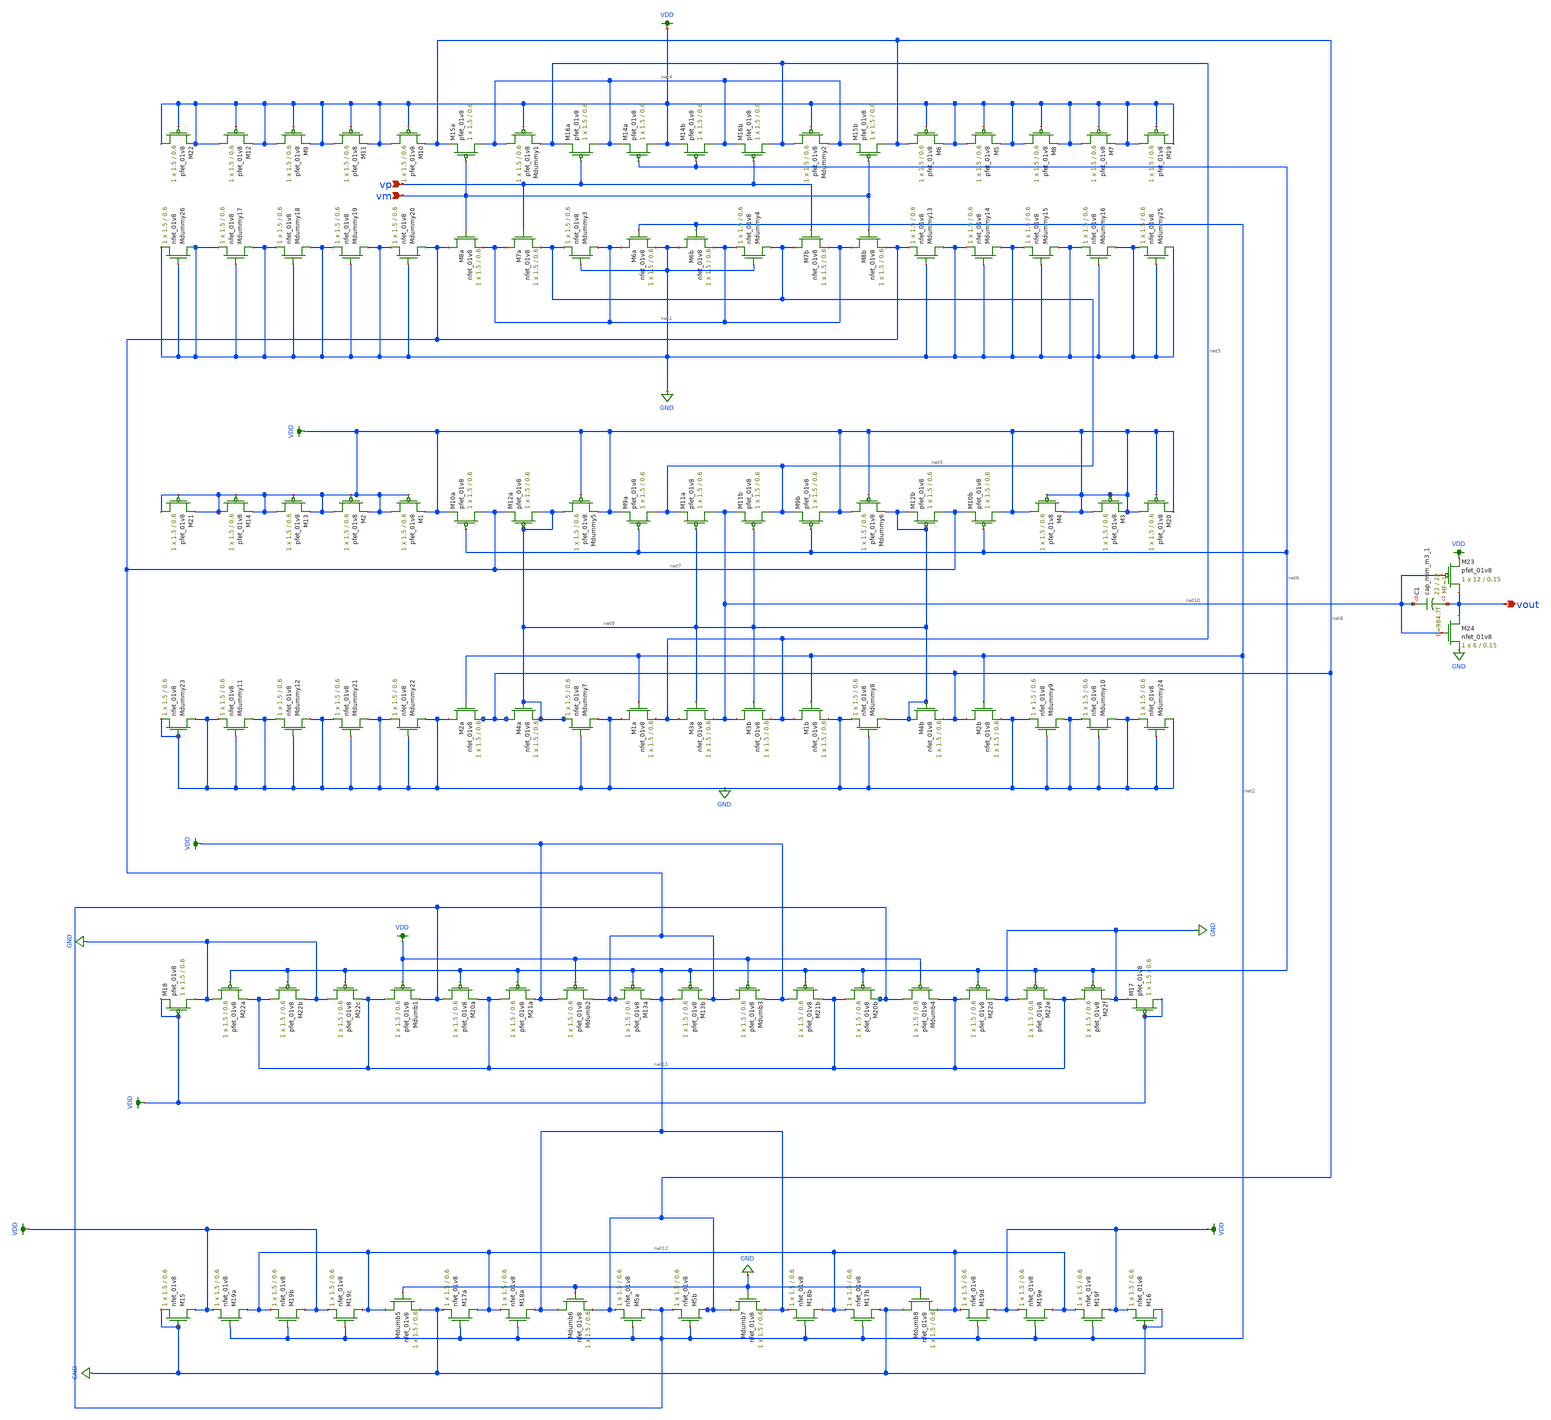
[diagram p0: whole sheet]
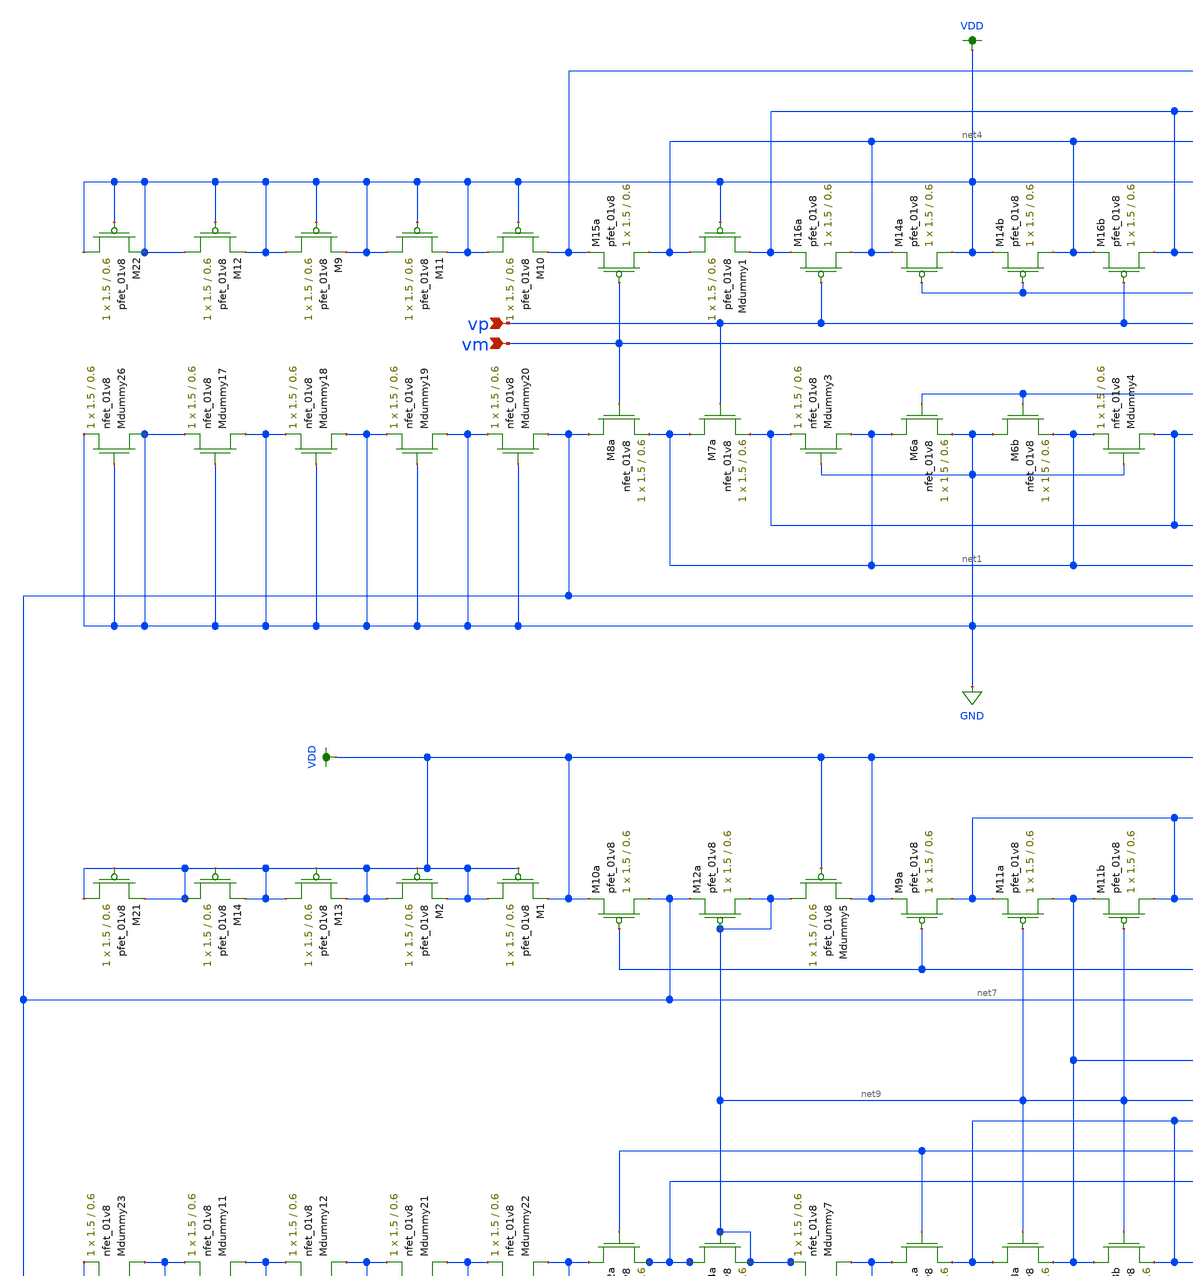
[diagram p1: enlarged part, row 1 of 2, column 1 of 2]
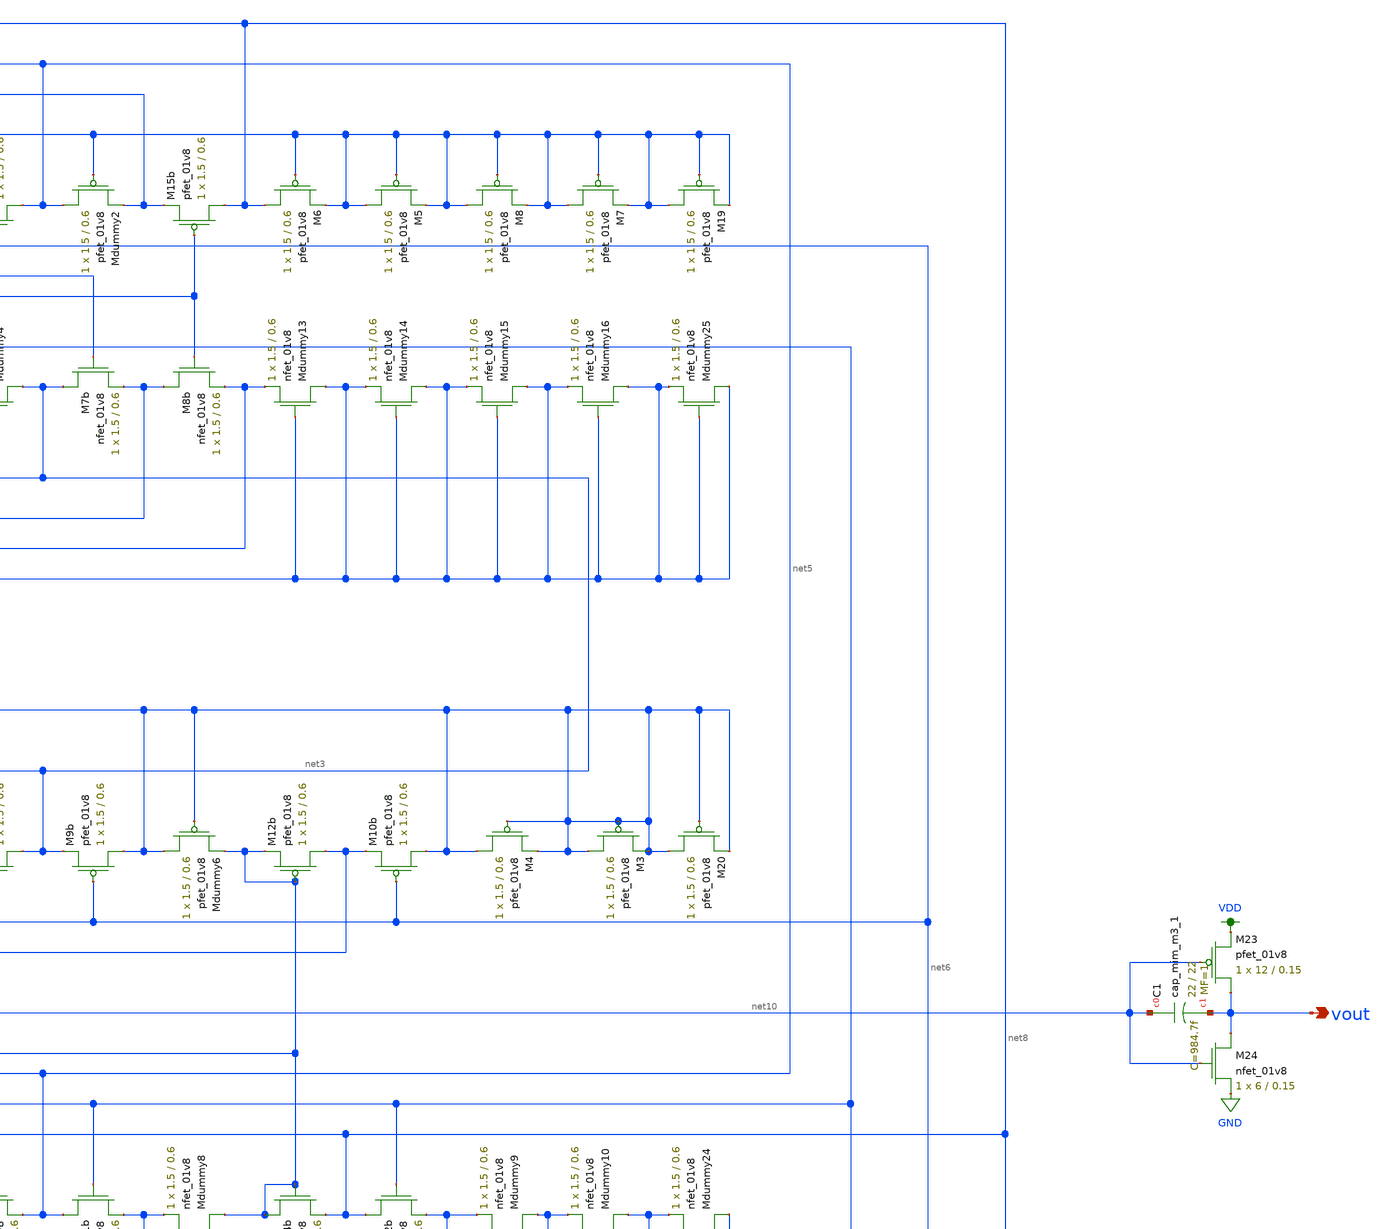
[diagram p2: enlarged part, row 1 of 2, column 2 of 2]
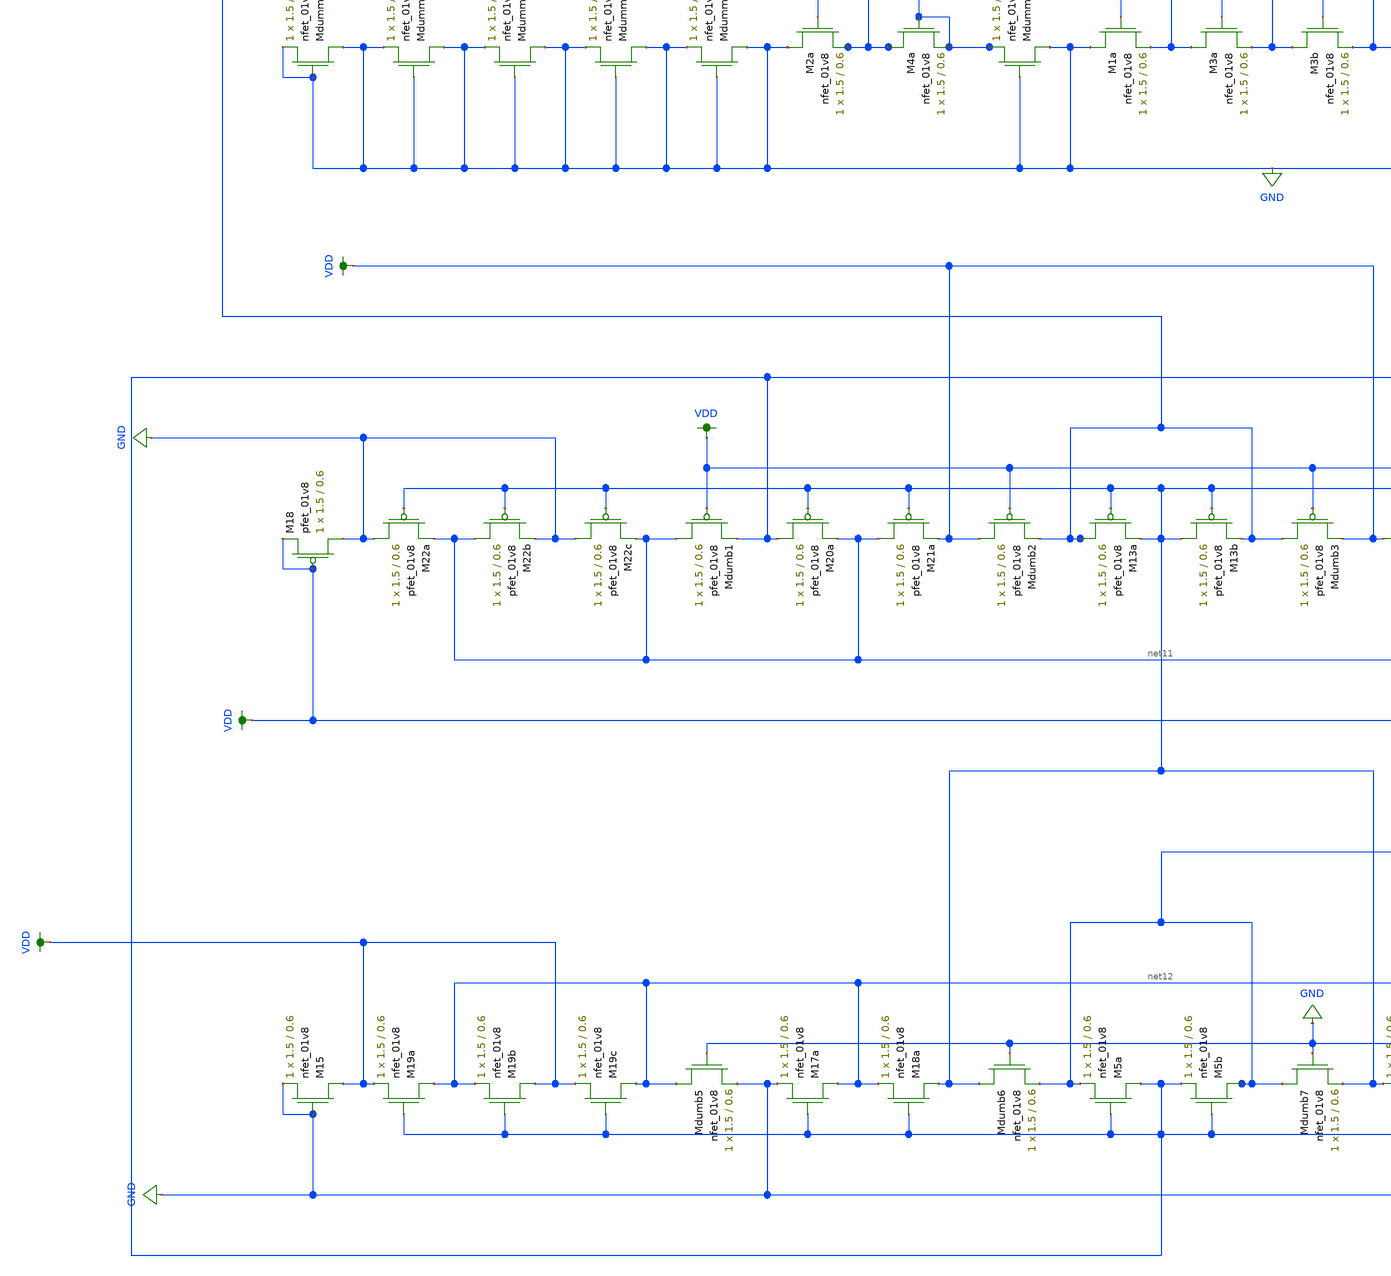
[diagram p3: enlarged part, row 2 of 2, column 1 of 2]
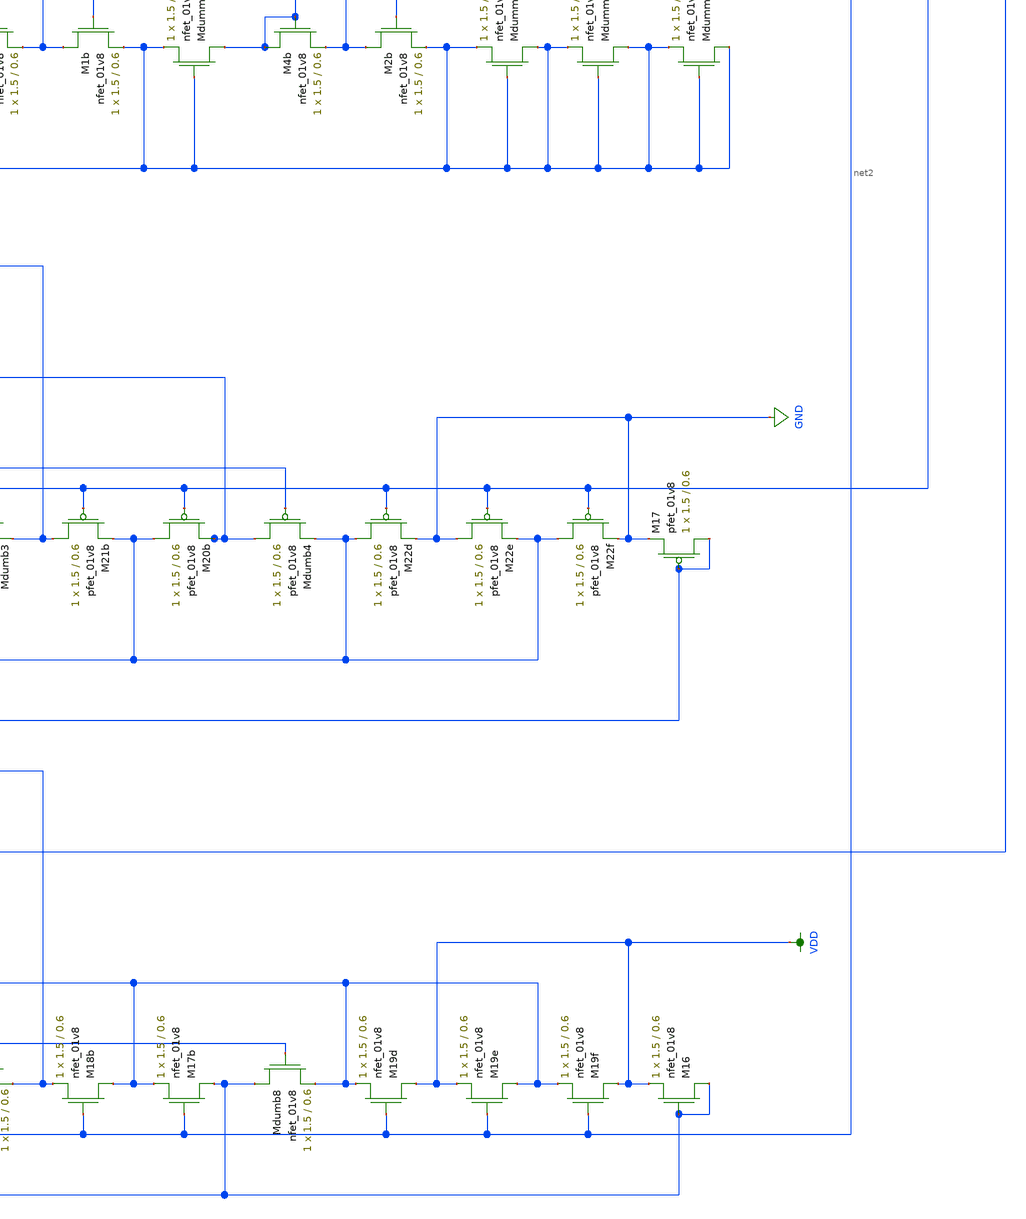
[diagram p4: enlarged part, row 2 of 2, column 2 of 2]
** sch_path: schematic/selfbiasedcascode2stage_lvs.sch
**.subckt selfbiasedcascode2stage_lvs vm vp vout
*.ipin vm
*.ipin vp
*.opin vout
XMdummy1 net4 VDD net5 VDD sky130_fd_pr__pfet_01v8 L=0.6 W=1.5 nf=1 ad='int((nf+1)/2) * W/nf * 0.29'
+ as='int((nf+2)/2) * W/nf * 0.29' pd='2*int((nf+1)/2) * (W/nf + 0.29)' ps='2*int((nf+2)/2) * (W/nf + 0.29)'
+ nrd='0.29 / W' nrs='0.29 / W' sa=0 sb=0 sd=0 mult=1 m=1
XM16a net4 vp net5 VDD sky130_fd_pr__pfet_01v8 L=0.6 W=1.5 nf=1 ad='int((nf+1)/2) * W/nf * 0.29' as='int((nf+2)/2) * W/nf * 0.29'
+ pd='2*int((nf+1)/2) * (W/nf + 0.29)' ps='2*int((nf+2)/2) * (W/nf + 0.29)' nrd='0.29 / W' nrs='0.29 / W'
+ sa=0 sb=0 sd=0 mult=1 m=1
XM14a VDD net6 net4 VDD sky130_fd_pr__pfet_01v8 L=0.6 W=1.5 nf=1 ad='int((nf+1)/2) * W/nf * 0.29' as='int((nf+2)/2) * W/nf * 0.29'
+ pd='2*int((nf+1)/2) * (W/nf + 0.29)' ps='2*int((nf+2)/2) * (W/nf + 0.29)' nrd='0.29 / W' nrs='0.29 / W'
+ sa=0 sb=0 sd=0 mult=1 m=1
XM14b net4 net6 VDD VDD sky130_fd_pr__pfet_01v8 L=0.6 W=1.5 nf=1 ad='int((nf+1)/2) * W/nf * 0.29' as='int((nf+2)/2) * W/nf * 0.29'
+ pd='2*int((nf+1)/2) * (W/nf + 0.29)' ps='2*int((nf+2)/2) * (W/nf + 0.29)' nrd='0.29 / W' nrs='0.29 / W'
+ sa=0 sb=0 sd=0 mult=1 m=1
XM15a net4 vm net8 VDD sky130_fd_pr__pfet_01v8 L=0.6 W=1.5 nf=1 ad='int((nf+1)/2) * W/nf * 0.29' as='int((nf+2)/2) * W/nf * 0.29'
+ pd='2*int((nf+1)/2) * (W/nf + 0.29)' ps='2*int((nf+2)/2) * (W/nf + 0.29)' nrd='0.29 / W' nrs='0.29 / W'
+ sa=0 sb=0 sd=0 mult=1 m=1
XM16b net5 vp net4 VDD sky130_fd_pr__pfet_01v8 L=0.6 W=1.5 nf=1 ad='int((nf+1)/2) * W/nf * 0.29' as='int((nf+2)/2) * W/nf * 0.29'
+ pd='2*int((nf+1)/2) * (W/nf + 0.29)' ps='2*int((nf+2)/2) * (W/nf + 0.29)' nrd='0.29 / W' nrs='0.29 / W'
+ sa=0 sb=0 sd=0 mult=1 m=1
XMdummy3 net1 GND net3 GND sky130_fd_pr__nfet_01v8 L=0.6 W=1.5 nf=1 ad='int((nf+1)/2) * W/nf * 0.29'
+ as='int((nf+2)/2) * W/nf * 0.29' pd='2*int((nf+1)/2) * (W/nf + 0.29)' ps='2*int((nf+2)/2) * (W/nf + 0.29)'
+ nrd='0.29 / W' nrs='0.29 / W' sa=0 sb=0 sd=0 mult=1 m=1
XM6a net1 net2 GND GND sky130_fd_pr__nfet_01v8 L=0.6 W=1.5 nf=1 ad='int((nf+1)/2) * W/nf * 0.29' as='int((nf+2)/2) * W/nf * 0.29'
+ pd='2*int((nf+1)/2) * (W/nf + 0.29)' ps='2*int((nf+2)/2) * (W/nf + 0.29)' nrd='0.29 / W' nrs='0.29 / W'
+ sa=0 sb=0 sd=0 mult=1 m=1
XM6b GND net2 net1 GND sky130_fd_pr__nfet_01v8 L=0.6 W=1.5 nf=1 ad='int((nf+1)/2) * W/nf * 0.29' as='int((nf+2)/2) * W/nf * 0.29'
+ pd='2*int((nf+1)/2) * (W/nf + 0.29)' ps='2*int((nf+2)/2) * (W/nf + 0.29)' nrd='0.29 / W' nrs='0.29 / W'
+ sa=0 sb=0 sd=0 mult=1 m=1
XMdummy4 net3 GND net1 GND sky130_fd_pr__nfet_01v8 L=0.6 W=1.5 nf=1 ad='int((nf+1)/2) * W/nf * 0.29'
+ as='int((nf+2)/2) * W/nf * 0.29' pd='2*int((nf+1)/2) * (W/nf + 0.29)' ps='2*int((nf+2)/2) * (W/nf + 0.29)'
+ nrd='0.29 / W' nrs='0.29 / W' sa=0 sb=0 sd=0 mult=1 m=1
XM8a net7 vm net1 GND sky130_fd_pr__nfet_01v8 L=0.6 W=1.5 nf=1 ad='int((nf+1)/2) * W/nf * 0.29' as='int((nf+2)/2) * W/nf * 0.29'
+ pd='2*int((nf+1)/2) * (W/nf + 0.29)' ps='2*int((nf+2)/2) * (W/nf + 0.29)' nrd='0.29 / W' nrs='0.29 / W'
+ sa=0 sb=0 sd=0 mult=1 m=1
XM7a net1 vp net3 GND sky130_fd_pr__nfet_01v8 L=0.6 W=1.5 nf=1 ad='int((nf+1)/2) * W/nf * 0.29' as='int((nf+2)/2) * W/nf * 0.29'
+ pd='2*int((nf+1)/2) * (W/nf + 0.29)' ps='2*int((nf+2)/2) * (W/nf + 0.29)' nrd='0.29 / W' nrs='0.29 / W'
+ sa=0 sb=0 sd=0 mult=1 m=1
XMdummy2 net5 VDD net4 VDD sky130_fd_pr__pfet_01v8 L=0.6 W=1.5 nf=1 ad='int((nf+1)/2) * W/nf * 0.29'
+ as='int((nf+2)/2) * W/nf * 0.29' pd='2*int((nf+1)/2) * (W/nf + 0.29)' ps='2*int((nf+2)/2) * (W/nf + 0.29)'
+ nrd='0.29 / W' nrs='0.29 / W' sa=0 sb=0 sd=0 mult=1 m=1
XM15b net8 vm net4 VDD sky130_fd_pr__pfet_01v8 L=0.6 W=1.5 nf=1 ad='int((nf+1)/2) * W/nf * 0.29' as='int((nf+2)/2) * W/nf * 0.29'
+ pd='2*int((nf+1)/2) * (W/nf + 0.29)' ps='2*int((nf+2)/2) * (W/nf + 0.29)' nrd='0.29 / W' nrs='0.29 / W'
+ sa=0 sb=0 sd=0 mult=1 m=1
XM7b net3 vp net1 GND sky130_fd_pr__nfet_01v8 L=0.6 W=1.5 nf=1 ad='int((nf+1)/2) * W/nf * 0.29' as='int((nf+2)/2) * W/nf * 0.29'
+ pd='2*int((nf+1)/2) * (W/nf + 0.29)' ps='2*int((nf+2)/2) * (W/nf + 0.29)' nrd='0.29 / W' nrs='0.29 / W'
+ sa=0 sb=0 sd=0 mult=1 m=1
XM8b net1 vm net7 GND sky130_fd_pr__nfet_01v8 L=0.6 W=1.5 nf=1 ad='int((nf+1)/2) * W/nf * 0.29' as='int((nf+2)/2) * W/nf * 0.29'
+ pd='2*int((nf+1)/2) * (W/nf + 0.29)' ps='2*int((nf+2)/2) * (W/nf + 0.29)' nrd='0.29 / W' nrs='0.29 / W'
+ sa=0 sb=0 sd=0 mult=1 m=1
XM10a net7 net6 VDD VDD sky130_fd_pr__pfet_01v8 L=0.6 W=1.5 nf=1 ad='int((nf+1)/2) * W/nf * 0.29' as='int((nf+2)/2) * W/nf * 0.29'
+ pd='2*int((nf+1)/2) * (W/nf + 0.29)' ps='2*int((nf+2)/2) * (W/nf + 0.29)' nrd='0.29 / W' nrs='0.29 / W'
+ sa=0 sb=0 sd=0 mult=1 m=1
XM9a net3 net6 VDD VDD sky130_fd_pr__pfet_01v8 L=0.6 W=1.5 nf=1 ad='int((nf+1)/2) * W/nf * 0.29' as='int((nf+2)/2) * W/nf * 0.29'
+ pd='2*int((nf+1)/2) * (W/nf + 0.29)' ps='2*int((nf+2)/2) * (W/nf + 0.29)' nrd='0.29 / W' nrs='0.29 / W'
+ sa=0 sb=0 sd=0 mult=1 m=1
XM12a net9 net9 net7 VDD sky130_fd_pr__pfet_01v8 L=0.6 W=1.5 nf=1 ad='int((nf+1)/2) * W/nf * 0.29' as='int((nf+2)/2) * W/nf * 0.29'
+ pd='2*int((nf+1)/2) * (W/nf + 0.29)' ps='2*int((nf+2)/2) * (W/nf + 0.29)' nrd='0.29 / W' nrs='0.29 / W'
+ sa=0 sb=0 sd=0 mult=1 m=1
XM11a net10 net9 net3 VDD sky130_fd_pr__pfet_01v8 L=0.6 W=1.5 nf=1 ad='int((nf+1)/2) * W/nf * 0.29' as='int((nf+2)/2) * W/nf * 0.29'
+ pd='2*int((nf+1)/2) * (W/nf + 0.29)' ps='2*int((nf+2)/2) * (W/nf + 0.29)' nrd='0.29 / W' nrs='0.29 / W'
+ sa=0 sb=0 sd=0 mult=1 m=1
XM11b net3 net9 net10 VDD sky130_fd_pr__pfet_01v8 L=0.6 W=1.5 nf=1 ad='int((nf+1)/2) * W/nf * 0.29' as='int((nf+2)/2) * W/nf * 0.29'
+ pd='2*int((nf+1)/2) * (W/nf + 0.29)' ps='2*int((nf+2)/2) * (W/nf + 0.29)' nrd='0.29 / W' nrs='0.29 / W'
+ sa=0 sb=0 sd=0 mult=1 m=1
XM12b net7 net9 net9 VDD sky130_fd_pr__pfet_01v8 L=0.6 W=1.5 nf=1 ad='int((nf+1)/2) * W/nf * 0.29' as='int((nf+2)/2) * W/nf * 0.29'
+ pd='2*int((nf+1)/2) * (W/nf + 0.29)' ps='2*int((nf+2)/2) * (W/nf + 0.29)' nrd='0.29 / W' nrs='0.29 / W'
+ sa=0 sb=0 sd=0 mult=1 m=1
XM9b VDD net6 net3 VDD sky130_fd_pr__pfet_01v8 L=0.6 W=1.5 nf=1 ad='int((nf+1)/2) * W/nf * 0.29' as='int((nf+2)/2) * W/nf * 0.29'
+ pd='2*int((nf+1)/2) * (W/nf + 0.29)' ps='2*int((nf+2)/2) * (W/nf + 0.29)' nrd='0.29 / W' nrs='0.29 / W'
+ sa=0 sb=0 sd=0 mult=1 m=1
XM10b VDD net6 net7 VDD sky130_fd_pr__pfet_01v8 L=0.6 W=1.5 nf=1 ad='int((nf+1)/2) * W/nf * 0.29' as='int((nf+2)/2) * W/nf * 0.29'
+ pd='2*int((nf+1)/2) * (W/nf + 0.29)' ps='2*int((nf+2)/2) * (W/nf + 0.29)' nrd='0.29 / W' nrs='0.29 / W'
+ sa=0 sb=0 sd=0 mult=1 m=1
XMdummy5 net9 VDD VDD VDD sky130_fd_pr__pfet_01v8 L=0.6 W=1.5 nf=1 ad='int((nf+1)/2) * W/nf * 0.29' as='int((nf+2)/2) * W/nf * 0.29'
+ pd='2*int((nf+1)/2) * (W/nf + 0.29)' ps='2*int((nf+2)/2) * (W/nf + 0.29)' nrd='0.29 / W' nrs='0.29 / W'
+ sa=0 sb=0 sd=0 mult=1 m=1
XMdummy6 VDD VDD net9 VDD sky130_fd_pr__pfet_01v8 L=0.6 W=1.5 nf=1 ad='int((nf+1)/2) * W/nf * 0.29' as='int((nf+2)/2) * W/nf * 0.29'
+ pd='2*int((nf+1)/2) * (W/nf + 0.29)' ps='2*int((nf+2)/2) * (W/nf + 0.29)' nrd='0.29 / W' nrs='0.29 / W'
+ sa=0 sb=0 sd=0 mult=1 m=1
XM2a GND net2 net8 GND sky130_fd_pr__nfet_01v8 L=0.6 W=1.5 nf=1 ad='int((nf+1)/2) * W/nf * 0.29' as='int((nf+2)/2) * W/nf * 0.29'
+ pd='2*int((nf+1)/2) * (W/nf + 0.29)' ps='2*int((nf+2)/2) * (W/nf + 0.29)' nrd='0.29 / W' nrs='0.29 / W'
+ sa=0 sb=0 sd=0 mult=1 m=1
XM4a net8 net9 net9 GND sky130_fd_pr__nfet_01v8 L=0.6 W=1.5 nf=1 ad='int((nf+1)/2) * W/nf * 0.29' as='int((nf+2)/2) * W/nf * 0.29'
+ pd='2*int((nf+1)/2) * (W/nf + 0.29)' ps='2*int((nf+2)/2) * (W/nf + 0.29)' nrd='0.29 / W' nrs='0.29 / W'
+ sa=0 sb=0 sd=0 mult=1 m=1
XMdummy7 GND GND net9 GND sky130_fd_pr__nfet_01v8 L=0.6 W=1.5 nf=1 ad='int((nf+1)/2) * W/nf * 0.29' as='int((nf+2)/2) * W/nf * 0.29'
+ pd='2*int((nf+1)/2) * (W/nf + 0.29)' ps='2*int((nf+2)/2) * (W/nf + 0.29)' nrd='0.29 / W' nrs='0.29 / W'
+ sa=0 sb=0 sd=0 mult=1 m=1
XM1a GND net2 net5 GND sky130_fd_pr__nfet_01v8 L=0.6 W=1.5 nf=1 ad='int((nf+1)/2) * W/nf * 0.29' as='int((nf+2)/2) * W/nf * 0.29'
+ pd='2*int((nf+1)/2) * (W/nf + 0.29)' ps='2*int((nf+2)/2) * (W/nf + 0.29)' nrd='0.29 / W' nrs='0.29 / W'
+ sa=0 sb=0 sd=0 mult=1 m=1
XM3a net5 net9 net10 GND sky130_fd_pr__nfet_01v8 L=0.6 W=1.5 nf=1 ad='int((nf+1)/2) * W/nf * 0.29' as='int((nf+2)/2) * W/nf * 0.29'
+ pd='2*int((nf+1)/2) * (W/nf + 0.29)' ps='2*int((nf+2)/2) * (W/nf + 0.29)' nrd='0.29 / W' nrs='0.29 / W'
+ sa=0 sb=0 sd=0 mult=1 m=1
XM3b net10 net9 net5 GND sky130_fd_pr__nfet_01v8 L=0.6 W=1.5 nf=1 ad='int((nf+1)/2) * W/nf * 0.29' as='int((nf+2)/2) * W/nf * 0.29'
+ pd='2*int((nf+1)/2) * (W/nf + 0.29)' ps='2*int((nf+2)/2) * (W/nf + 0.29)' nrd='0.29 / W' nrs='0.29 / W'
+ sa=0 sb=0 sd=0 mult=1 m=1
XM1b net5 net2 GND GND sky130_fd_pr__nfet_01v8 L=0.6 W=1.5 nf=1 ad='int((nf+1)/2) * W/nf * 0.29' as='int((nf+2)/2) * W/nf * 0.29'
+ pd='2*int((nf+1)/2) * (W/nf + 0.29)' ps='2*int((nf+2)/2) * (W/nf + 0.29)' nrd='0.29 / W' nrs='0.29 / W'
+ sa=0 sb=0 sd=0 mult=1 m=1
XMdummy8 net9 GND GND GND sky130_fd_pr__nfet_01v8 L=0.6 W=1.5 nf=1 ad='int((nf+1)/2) * W/nf * 0.29' as='int((nf+2)/2) * W/nf * 0.29'
+ pd='2*int((nf+1)/2) * (W/nf + 0.29)' ps='2*int((nf+2)/2) * (W/nf + 0.29)' nrd='0.29 / W' nrs='0.29 / W'
+ sa=0 sb=0 sd=0 mult=1 m=1
XM4b net9 net9 net8 GND sky130_fd_pr__nfet_01v8 L=0.6 W=1.5 nf=1 ad='int((nf+1)/2) * W/nf * 0.29' as='int((nf+2)/2) * W/nf * 0.29'
+ pd='2*int((nf+1)/2) * (W/nf + 0.29)' ps='2*int((nf+2)/2) * (W/nf + 0.29)' nrd='0.29 / W' nrs='0.29 / W'
+ sa=0 sb=0 sd=0 mult=1 m=1
XM2b net8 net2 GND GND sky130_fd_pr__nfet_01v8 L=0.6 W=1.5 nf=1 ad='int((nf+1)/2) * W/nf * 0.29' as='int((nf+2)/2) * W/nf * 0.29'
+ pd='2*int((nf+1)/2) * (W/nf + 0.29)' ps='2*int((nf+2)/2) * (W/nf + 0.29)' nrd='0.29 / W' nrs='0.29 / W'
+ sa=0 sb=0 sd=0 mult=1 m=1
XM13a net7 net6 net6 VDD sky130_fd_pr__pfet_01v8 L=0.6 W=1.5 nf=1 ad='int((nf+1)/2) * W/nf * 0.29' as='int((nf+2)/2) * W/nf * 0.29'
+ pd='2*int((nf+1)/2) * (W/nf + 0.29)' ps='2*int((nf+2)/2) * (W/nf + 0.29)' nrd='0.29 / W' nrs='0.29 / W'
+ sa=0 sb=0 sd=0 mult=1 m=1
XM21a net11 net6 VDD VDD sky130_fd_pr__pfet_01v8 L=0.6 W=1.5 nf=1 ad='int((nf+1)/2) * W/nf * 0.29' as='int((nf+2)/2) * W/nf * 0.29'
+ pd='2*int((nf+1)/2) * (W/nf + 0.29)' ps='2*int((nf+2)/2) * (W/nf + 0.29)' nrd='0.29 / W' nrs='0.29 / W'
+ sa=0 sb=0 sd=0 mult=1 m=1
XM22c GND net6 net11 VDD sky130_fd_pr__pfet_01v8 L=0.6 W=1.5 nf=1 ad='int((nf+1)/2) * W/nf * 0.29' as='int((nf+2)/2) * W/nf * 0.29'
+ pd='2*int((nf+1)/2) * (W/nf + 0.29)' ps='2*int((nf+2)/2) * (W/nf + 0.29)' nrd='0.29 / W' nrs='0.29 / W'
+ sa=0 sb=0 sd=0 mult=1 m=1
XM20a net2 net6 net11 VDD sky130_fd_pr__pfet_01v8 L=0.6 W=1.5 nf=1 ad='int((nf+1)/2) * W/nf * 0.29' as='int((nf+2)/2) * W/nf * 0.29'
+ pd='2*int((nf+1)/2) * (W/nf + 0.29)' ps='2*int((nf+2)/2) * (W/nf + 0.29)' nrd='0.29 / W' nrs='0.29 / W'
+ sa=0 sb=0 sd=0 mult=1 m=1
XM22a GND net6 net11 VDD sky130_fd_pr__pfet_01v8 L=0.6 W=1.5 nf=1 ad='int((nf+1)/2) * W/nf * 0.29' as='int((nf+2)/2) * W/nf * 0.29'
+ pd='2*int((nf+1)/2) * (W/nf + 0.29)' ps='2*int((nf+2)/2) * (W/nf + 0.29)' nrd='0.29 / W' nrs='0.29 / W'
+ sa=0 sb=0 sd=0 mult=1 m=1
XM22b net11 net6 GND VDD sky130_fd_pr__pfet_01v8 L=0.6 W=1.5 nf=1 ad='int((nf+1)/2) * W/nf * 0.29' as='int((nf+2)/2) * W/nf * 0.29'
+ pd='2*int((nf+1)/2) * (W/nf + 0.29)' ps='2*int((nf+2)/2) * (W/nf + 0.29)' nrd='0.29 / W' nrs='0.29 / W'
+ sa=0 sb=0 sd=0 mult=1 m=1
XM22f net11 net6 GND VDD sky130_fd_pr__pfet_01v8 L=0.6 W=1.5 nf=1 ad='int((nf+1)/2) * W/nf * 0.29' as='int((nf+2)/2) * W/nf * 0.29'
+ pd='2*int((nf+1)/2) * (W/nf + 0.29)' ps='2*int((nf+2)/2) * (W/nf + 0.29)' nrd='0.29 / W' nrs='0.29 / W'
+ sa=0 sb=0 sd=0 mult=1 m=1
XM22e GND net6 net11 VDD sky130_fd_pr__pfet_01v8 L=0.6 W=1.5 nf=1 ad='int((nf+1)/2) * W/nf * 0.29' as='int((nf+2)/2) * W/nf * 0.29'
+ pd='2*int((nf+1)/2) * (W/nf + 0.29)' ps='2*int((nf+2)/2) * (W/nf + 0.29)' nrd='0.29 / W' nrs='0.29 / W'
+ sa=0 sb=0 sd=0 mult=1 m=1
XM20b net11 net6 net2 VDD sky130_fd_pr__pfet_01v8 L=0.6 W=1.5 nf=1 ad='int((nf+1)/2) * W/nf * 0.29' as='int((nf+2)/2) * W/nf * 0.29'
+ pd='2*int((nf+1)/2) * (W/nf + 0.29)' ps='2*int((nf+2)/2) * (W/nf + 0.29)' nrd='0.29 / W' nrs='0.29 / W'
+ sa=0 sb=0 sd=0 mult=1 m=1
XM22d net11 net6 GND VDD sky130_fd_pr__pfet_01v8 L=0.6 W=1.5 nf=1 ad='int((nf+1)/2) * W/nf * 0.29' as='int((nf+2)/2) * W/nf * 0.29'
+ pd='2*int((nf+1)/2) * (W/nf + 0.29)' ps='2*int((nf+2)/2) * (W/nf + 0.29)' nrd='0.29 / W' nrs='0.29 / W'
+ sa=0 sb=0 sd=0 mult=1 m=1
XM13b net6 net6 net7 VDD sky130_fd_pr__pfet_01v8 L=0.6 W=1.5 nf=1 ad='int((nf+1)/2) * W/nf * 0.29' as='int((nf+2)/2) * W/nf * 0.29'
+ pd='2*int((nf+1)/2) * (W/nf + 0.29)' ps='2*int((nf+2)/2) * (W/nf + 0.29)' nrd='0.29 / W' nrs='0.29 / W'
+ sa=0 sb=0 sd=0 mult=1 m=1
XM21b VDD net6 net11 VDD sky130_fd_pr__pfet_01v8 L=0.6 W=1.5 nf=1 ad='int((nf+1)/2) * W/nf * 0.29' as='int((nf+2)/2) * W/nf * 0.29'
+ pd='2*int((nf+1)/2) * (W/nf + 0.29)' ps='2*int((nf+2)/2) * (W/nf + 0.29)' nrd='0.29 / W' nrs='0.29 / W'
+ sa=0 sb=0 sd=0 mult=1 m=1
XM5a net2 net2 net8 GND sky130_fd_pr__nfet_01v8 L=0.6 W=1.5 nf=1 ad='int((nf+1)/2) * W/nf * 0.29' as='int((nf+2)/2) * W/nf * 0.29'
+ pd='2*int((nf+1)/2) * (W/nf + 0.29)' ps='2*int((nf+2)/2) * (W/nf + 0.29)' nrd='0.29 / W' nrs='0.29 / W'
+ sa=0 sb=0 sd=0 mult=1 m=1
XM18a net6 net2 net12 GND sky130_fd_pr__nfet_01v8 L=0.6 W=1.5 nf=1 ad='int((nf+1)/2) * W/nf * 0.29' as='int((nf+2)/2) * W/nf * 0.29'
+ pd='2*int((nf+1)/2) * (W/nf + 0.29)' ps='2*int((nf+2)/2) * (W/nf + 0.29)' nrd='0.29 / W' nrs='0.29 / W'
+ sa=0 sb=0 sd=0 mult=1 m=1
XM17a net12 net2 GND GND sky130_fd_pr__nfet_01v8 L=0.6 W=1.5 nf=1 ad='int((nf+1)/2) * W/nf * 0.29' as='int((nf+2)/2) * W/nf * 0.29'
+ pd='2*int((nf+1)/2) * (W/nf + 0.29)' ps='2*int((nf+2)/2) * (W/nf + 0.29)' nrd='0.29 / W' nrs='0.29 / W'
+ sa=0 sb=0 sd=0 mult=1 m=1
XM19c net12 net2 VDD GND sky130_fd_pr__nfet_01v8 L=0.6 W=1.5 nf=1 ad='int((nf+1)/2) * W/nf * 0.29' as='int((nf+2)/2) * W/nf * 0.29'
+ pd='2*int((nf+1)/2) * (W/nf + 0.29)' ps='2*int((nf+2)/2) * (W/nf + 0.29)' nrd='0.29 / W' nrs='0.29 / W'
+ sa=0 sb=0 sd=0 mult=1 m=1
XM19b VDD net2 net12 GND sky130_fd_pr__nfet_01v8 L=0.6 W=1.5 nf=1 ad='int((nf+1)/2) * W/nf * 0.29' as='int((nf+2)/2) * W/nf * 0.29'
+ pd='2*int((nf+1)/2) * (W/nf + 0.29)' ps='2*int((nf+2)/2) * (W/nf + 0.29)' nrd='0.29 / W' nrs='0.29 / W'
+ sa=0 sb=0 sd=0 mult=1 m=1
XM19a net12 net2 VDD GND sky130_fd_pr__nfet_01v8 L=0.6 W=1.5 nf=1 ad='int((nf+1)/2) * W/nf * 0.29' as='int((nf+2)/2) * W/nf * 0.29'
+ pd='2*int((nf+1)/2) * (W/nf + 0.29)' ps='2*int((nf+2)/2) * (W/nf + 0.29)' nrd='0.29 / W' nrs='0.29 / W'
+ sa=0 sb=0 sd=0 mult=1 m=1
XM19f VDD net2 net12 GND sky130_fd_pr__nfet_01v8 L=0.6 W=1.5 nf=1 ad='int((nf+1)/2) * W/nf * 0.29' as='int((nf+2)/2) * W/nf * 0.29'
+ pd='2*int((nf+1)/2) * (W/nf + 0.29)' ps='2*int((nf+2)/2) * (W/nf + 0.29)' nrd='0.29 / W' nrs='0.29 / W'
+ sa=0 sb=0 sd=0 mult=1 m=1
XM19e net12 net2 VDD GND sky130_fd_pr__nfet_01v8 L=0.6 W=1.5 nf=1 ad='int((nf+1)/2) * W/nf * 0.29' as='int((nf+2)/2) * W/nf * 0.29'
+ pd='2*int((nf+1)/2) * (W/nf + 0.29)' ps='2*int((nf+2)/2) * (W/nf + 0.29)' nrd='0.29 / W' nrs='0.29 / W'
+ sa=0 sb=0 sd=0 mult=1 m=1
XM19d VDD net2 net12 GND sky130_fd_pr__nfet_01v8 L=0.6 W=1.5 nf=1 ad='int((nf+1)/2) * W/nf * 0.29' as='int((nf+2)/2) * W/nf * 0.29'
+ pd='2*int((nf+1)/2) * (W/nf + 0.29)' ps='2*int((nf+2)/2) * (W/nf + 0.29)' nrd='0.29 / W' nrs='0.29 / W'
+ sa=0 sb=0 sd=0 mult=1 m=1
XM17b GND net2 net12 GND sky130_fd_pr__nfet_01v8 L=0.6 W=1.5 nf=1 ad='int((nf+1)/2) * W/nf * 0.29' as='int((nf+2)/2) * W/nf * 0.29'
+ pd='2*int((nf+1)/2) * (W/nf + 0.29)' ps='2*int((nf+2)/2) * (W/nf + 0.29)' nrd='0.29 / W' nrs='0.29 / W'
+ sa=0 sb=0 sd=0 mult=1 m=1
XM18b net12 net2 net6 GND sky130_fd_pr__nfet_01v8 L=0.6 W=1.5 nf=1 ad='int((nf+1)/2) * W/nf * 0.29' as='int((nf+2)/2) * W/nf * 0.29'
+ pd='2*int((nf+1)/2) * (W/nf + 0.29)' ps='2*int((nf+2)/2) * (W/nf + 0.29)' nrd='0.29 / W' nrs='0.29 / W'
+ sa=0 sb=0 sd=0 mult=1 m=1
XM5b net8 net2 net2 GND sky130_fd_pr__nfet_01v8 L=0.6 W=1.5 nf=1 ad='int((nf+1)/2) * W/nf * 0.29' as='int((nf+2)/2) * W/nf * 0.29'
+ pd='2*int((nf+1)/2) * (W/nf + 0.29)' ps='2*int((nf+2)/2) * (W/nf + 0.29)' nrd='0.29 / W' nrs='0.29 / W'
+ sa=0 sb=0 sd=0 mult=1 m=1
XMdumb1 net11 VDD net2 VDD sky130_fd_pr__pfet_01v8 L=0.6 W=1.5 nf=1 ad='int((nf+1)/2) * W/nf * 0.29'
+ as='int((nf+2)/2) * W/nf * 0.29' pd='2*int((nf+1)/2) * (W/nf + 0.29)' ps='2*int((nf+2)/2) * (W/nf + 0.29)'
+ nrd='0.29 / W' nrs='0.29 / W' sa=0 sb=0 sd=0 mult=1 m=1
XMdumb2 VDD VDD net7 VDD sky130_fd_pr__pfet_01v8 L=0.6 W=1.5 nf=1 ad='int((nf+1)/2) * W/nf * 0.29' as='int((nf+2)/2) * W/nf * 0.29'
+ pd='2*int((nf+1)/2) * (W/nf + 0.29)' ps='2*int((nf+2)/2) * (W/nf + 0.29)' nrd='0.29 / W' nrs='0.29 / W'
+ sa=0 sb=0 sd=0 mult=1 m=1
XMdumb3 net7 VDD VDD VDD sky130_fd_pr__pfet_01v8 L=0.6 W=1.5 nf=1 ad='int((nf+1)/2) * W/nf * 0.29' as='int((nf+2)/2) * W/nf * 0.29'
+ pd='2*int((nf+1)/2) * (W/nf + 0.29)' ps='2*int((nf+2)/2) * (W/nf + 0.29)' nrd='0.29 / W' nrs='0.29 / W'
+ sa=0 sb=0 sd=0 mult=1 m=1
XMdumb4 net2 VDD net11 VDD sky130_fd_pr__pfet_01v8 L=0.6 W=1.5 nf=1 ad='int((nf+1)/2) * W/nf * 0.29'
+ as='int((nf+2)/2) * W/nf * 0.29' pd='2*int((nf+1)/2) * (W/nf + 0.29)' ps='2*int((nf+2)/2) * (W/nf + 0.29)'
+ nrd='0.29 / W' nrs='0.29 / W' sa=0 sb=0 sd=0 mult=1 m=1
XMdumb5 net12 GND GND GND sky130_fd_pr__nfet_01v8 L=0.6 W=1.5 nf=1 ad='int((nf+1)/2) * W/nf * 0.29' as='int((nf+2)/2) * W/nf * 0.29'
+ pd='2*int((nf+1)/2) * (W/nf + 0.29)' ps='2*int((nf+2)/2) * (W/nf + 0.29)' nrd='0.29 / W' nrs='0.29 / W'
+ sa=0 sb=0 sd=0 mult=1 m=1
XMdumb6 net6 GND net8 GND sky130_fd_pr__nfet_01v8 L=0.6 W=1.5 nf=1 ad='int((nf+1)/2) * W/nf * 0.29' as='int((nf+2)/2) * W/nf * 0.29'
+ pd='2*int((nf+1)/2) * (W/nf + 0.29)' ps='2*int((nf+2)/2) * (W/nf + 0.29)' nrd='0.29 / W' nrs='0.29 / W'
+ sa=0 sb=0 sd=0 mult=1 m=1
XMdumb7 net8 GND net6 GND sky130_fd_pr__nfet_01v8 L=0.6 W=1.5 nf=1 ad='int((nf+1)/2) * W/nf * 0.29' as='int((nf+2)/2) * W/nf * 0.29'
+ pd='2*int((nf+1)/2) * (W/nf + 0.29)' ps='2*int((nf+2)/2) * (W/nf + 0.29)' nrd='0.29 / W' nrs='0.29 / W'
+ sa=0 sb=0 sd=0 mult=1 m=1
XMdumb8 GND GND net12 GND sky130_fd_pr__nfet_01v8 L=0.6 W=1.5 nf=1 ad='int((nf+1)/2) * W/nf * 0.29' as='int((nf+2)/2) * W/nf * 0.29'
+ pd='2*int((nf+1)/2) * (W/nf + 0.29)' ps='2*int((nf+2)/2) * (W/nf + 0.29)' nrd='0.29 / W' nrs='0.29 / W'
+ sa=0 sb=0 sd=0 mult=1 m=1
XMdummy9 GND GND GND GND sky130_fd_pr__nfet_01v8 L=0.6 W=1.5 nf=1 ad='int((nf+1)/2) * W/nf * 0.29' as='int((nf+2)/2) * W/nf * 0.29'
+ pd='2*int((nf+1)/2) * (W/nf + 0.29)' ps='2*int((nf+2)/2) * (W/nf + 0.29)' nrd='0.29 / W' nrs='0.29 / W'
+ sa=0 sb=0 sd=0 mult=1 m=1
XMdummy10 GND GND GND GND sky130_fd_pr__nfet_01v8 L=0.6 W=1.5 nf=1 ad='int((nf+1)/2) * W/nf * 0.29' as='int((nf+2)/2) * W/nf * 0.29'
+ pd='2*int((nf+1)/2) * (W/nf + 0.29)' ps='2*int((nf+2)/2) * (W/nf + 0.29)' nrd='0.29 / W' nrs='0.29 / W'
+ sa=0 sb=0 sd=0 mult=1 m=1
XM1 VDD VDD VDD VDD sky130_fd_pr__pfet_01v8 L=0.6 W=1.5 nf=1 ad='int((nf+1)/2) * W/nf * 0.29' as='int((nf+2)/2) * W/nf * 0.29'
+ pd='2*int((nf+1)/2) * (W/nf + 0.29)' ps='2*int((nf+2)/2) * (W/nf + 0.29)' nrd='0.29 / W' nrs='0.29 / W'
+ sa=0 sb=0 sd=0 mult=1 m=1
XM2 VDD VDD VDD VDD sky130_fd_pr__pfet_01v8 L=0.6 W=1.5 nf=1 ad='int((nf+1)/2) * W/nf * 0.29' as='int((nf+2)/2) * W/nf * 0.29'
+ pd='2*int((nf+1)/2) * (W/nf + 0.29)' ps='2*int((nf+2)/2) * (W/nf + 0.29)' nrd='0.29 / W' nrs='0.29 / W'
+ sa=0 sb=0 sd=0 mult=1 m=1
XM3 VDD VDD VDD VDD sky130_fd_pr__pfet_01v8 L=0.6 W=1.5 nf=1 ad='int((nf+1)/2) * W/nf * 0.29' as='int((nf+2)/2) * W/nf * 0.29'
+ pd='2*int((nf+1)/2) * (W/nf + 0.29)' ps='2*int((nf+2)/2) * (W/nf + 0.29)' nrd='0.29 / W' nrs='0.29 / W'
+ sa=0 sb=0 sd=0 mult=1 m=1
XM4 VDD VDD VDD VDD sky130_fd_pr__pfet_01v8 L=0.6 W=1.5 nf=1 ad='int((nf+1)/2) * W/nf * 0.29' as='int((nf+2)/2) * W/nf * 0.29'
+ pd='2*int((nf+1)/2) * (W/nf + 0.29)' ps='2*int((nf+2)/2) * (W/nf + 0.29)' nrd='0.29 / W' nrs='0.29 / W'
+ sa=0 sb=0 sd=0 mult=1 m=1
XM5 VDD VDD VDD VDD sky130_fd_pr__pfet_01v8 L=0.6 W=1.5 nf=1 ad='int((nf+1)/2) * W/nf * 0.29' as='int((nf+2)/2) * W/nf * 0.29'
+ pd='2*int((nf+1)/2) * (W/nf + 0.29)' ps='2*int((nf+2)/2) * (W/nf + 0.29)' nrd='0.29 / W' nrs='0.29 / W'
+ sa=0 sb=0 sd=0 mult=1 m=1
XM6 net8 VDD VDD VDD sky130_fd_pr__pfet_01v8 L=0.6 W=1.5 nf=1 ad='int((nf+1)/2) * W/nf * 0.29' as='int((nf+2)/2) * W/nf * 0.29'
+ pd='2*int((nf+1)/2) * (W/nf + 0.29)' ps='2*int((nf+2)/2) * (W/nf + 0.29)' nrd='0.29 / W' nrs='0.29 / W'
+ sa=0 sb=0 sd=0 mult=1 m=1
XM7 VDD VDD VDD VDD sky130_fd_pr__pfet_01v8 L=0.6 W=1.5 nf=1 ad='int((nf+1)/2) * W/nf * 0.29' as='int((nf+2)/2) * W/nf * 0.29'
+ pd='2*int((nf+1)/2) * (W/nf + 0.29)' ps='2*int((nf+2)/2) * (W/nf + 0.29)' nrd='0.29 / W' nrs='0.29 / W'
+ sa=0 sb=0 sd=0 mult=1 m=1
XM8 VDD VDD VDD VDD sky130_fd_pr__pfet_01v8 L=0.6 W=1.5 nf=1 ad='int((nf+1)/2) * W/nf * 0.29' as='int((nf+2)/2) * W/nf * 0.29'
+ pd='2*int((nf+1)/2) * (W/nf + 0.29)' ps='2*int((nf+2)/2) * (W/nf + 0.29)' nrd='0.29 / W' nrs='0.29 / W'
+ sa=0 sb=0 sd=0 mult=1 m=1
XMdummy13 GND GND net7 GND sky130_fd_pr__nfet_01v8 L=0.6 W=1.5 nf=1 ad='int((nf+1)/2) * W/nf * 0.29'
+ as='int((nf+2)/2) * W/nf * 0.29' pd='2*int((nf+1)/2) * (W/nf + 0.29)' ps='2*int((nf+2)/2) * (W/nf + 0.29)'
+ nrd='0.29 / W' nrs='0.29 / W' sa=0 sb=0 sd=0 mult=1 m=1
XMdummy14 GND GND GND GND sky130_fd_pr__nfet_01v8 L=0.6 W=1.5 nf=1 ad='int((nf+1)/2) * W/nf * 0.29' as='int((nf+2)/2) * W/nf * 0.29'
+ pd='2*int((nf+1)/2) * (W/nf + 0.29)' ps='2*int((nf+2)/2) * (W/nf + 0.29)' nrd='0.29 / W' nrs='0.29 / W'
+ sa=0 sb=0 sd=0 mult=1 m=1
XMdummy15 GND GND GND GND sky130_fd_pr__nfet_01v8 L=0.6 W=1.5 nf=1 ad='int((nf+1)/2) * W/nf * 0.29' as='int((nf+2)/2) * W/nf * 0.29'
+ pd='2*int((nf+1)/2) * (W/nf + 0.29)' ps='2*int((nf+2)/2) * (W/nf + 0.29)' nrd='0.29 / W' nrs='0.29 / W'
+ sa=0 sb=0 sd=0 mult=1 m=1
XMdummy16 GND GND GND GND sky130_fd_pr__nfet_01v8 L=0.6 W=1.5 nf=1 ad='int((nf+1)/2) * W/nf * 0.29' as='int((nf+2)/2) * W/nf * 0.29'
+ pd='2*int((nf+1)/2) * (W/nf + 0.29)' ps='2*int((nf+2)/2) * (W/nf + 0.29)' nrd='0.29 / W' nrs='0.29 / W'
+ sa=0 sb=0 sd=0 mult=1 m=1
XMdummy17 GND GND GND GND sky130_fd_pr__nfet_01v8 L=0.6 W=1.5 nf=1 ad='int((nf+1)/2) * W/nf * 0.29' as='int((nf+2)/2) * W/nf * 0.29'
+ pd='2*int((nf+1)/2) * (W/nf + 0.29)' ps='2*int((nf+2)/2) * (W/nf + 0.29)' nrd='0.29 / W' nrs='0.29 / W'
+ sa=0 sb=0 sd=0 mult=1 m=1
XMdummy18 GND GND GND GND sky130_fd_pr__nfet_01v8 L=0.6 W=1.5 nf=1 ad='int((nf+1)/2) * W/nf * 0.29' as='int((nf+2)/2) * W/nf * 0.29'
+ pd='2*int((nf+1)/2) * (W/nf + 0.29)' ps='2*int((nf+2)/2) * (W/nf + 0.29)' nrd='0.29 / W' nrs='0.29 / W'
+ sa=0 sb=0 sd=0 mult=1 m=1
XMdummy19 GND GND GND GND sky130_fd_pr__nfet_01v8 L=0.6 W=1.5 nf=1 ad='int((nf+1)/2) * W/nf * 0.29' as='int((nf+2)/2) * W/nf * 0.29'
+ pd='2*int((nf+1)/2) * (W/nf + 0.29)' ps='2*int((nf+2)/2) * (W/nf + 0.29)' nrd='0.29 / W' nrs='0.29 / W'
+ sa=0 sb=0 sd=0 mult=1 m=1
XMdummy20 net7 GND GND GND sky130_fd_pr__nfet_01v8 L=0.6 W=1.5 nf=1 ad='int((nf+1)/2) * W/nf * 0.29'
+ as='int((nf+2)/2) * W/nf * 0.29' pd='2*int((nf+1)/2) * (W/nf + 0.29)' ps='2*int((nf+2)/2) * (W/nf + 0.29)'
+ nrd='0.29 / W' nrs='0.29 / W' sa=0 sb=0 sd=0 mult=1 m=1
XM9 VDD VDD VDD VDD sky130_fd_pr__pfet_01v8 L=0.6 W=1.5 nf=1 ad='int((nf+1)/2) * W/nf * 0.29' as='int((nf+2)/2) * W/nf * 0.29'
+ pd='2*int((nf+1)/2) * (W/nf + 0.29)' ps='2*int((nf+2)/2) * (W/nf + 0.29)' nrd='0.29 / W' nrs='0.29 / W'
+ sa=0 sb=0 sd=0 mult=1 m=1
XM10 VDD VDD net8 VDD sky130_fd_pr__pfet_01v8 L=0.6 W=1.5 nf=1 ad='int((nf+1)/2) * W/nf * 0.29' as='int((nf+2)/2) * W/nf * 0.29'
+ pd='2*int((nf+1)/2) * (W/nf + 0.29)' ps='2*int((nf+2)/2) * (W/nf + 0.29)' nrd='0.29 / W' nrs='0.29 / W'
+ sa=0 sb=0 sd=0 mult=1 m=1
XM11 VDD VDD VDD VDD sky130_fd_pr__pfet_01v8 L=0.6 W=1.5 nf=1 ad='int((nf+1)/2) * W/nf * 0.29' as='int((nf+2)/2) * W/nf * 0.29'
+ pd='2*int((nf+1)/2) * (W/nf + 0.29)' ps='2*int((nf+2)/2) * (W/nf + 0.29)' nrd='0.29 / W' nrs='0.29 / W'
+ sa=0 sb=0 sd=0 mult=1 m=1
XM12 VDD VDD VDD VDD sky130_fd_pr__pfet_01v8 L=0.6 W=1.5 nf=1 ad='int((nf+1)/2) * W/nf * 0.29' as='int((nf+2)/2) * W/nf * 0.29'
+ pd='2*int((nf+1)/2) * (W/nf + 0.29)' ps='2*int((nf+2)/2) * (W/nf + 0.29)' nrd='0.29 / W' nrs='0.29 / W'
+ sa=0 sb=0 sd=0 mult=1 m=1
XM13 VDD VDD VDD VDD sky130_fd_pr__pfet_01v8 L=0.6 W=1.5 nf=1 ad='int((nf+1)/2) * W/nf * 0.29' as='int((nf+2)/2) * W/nf * 0.29'
+ pd='2*int((nf+1)/2) * (W/nf + 0.29)' ps='2*int((nf+2)/2) * (W/nf + 0.29)' nrd='0.29 / W' nrs='0.29 / W'
+ sa=0 sb=0 sd=0 mult=1 m=1
XM14 VDD VDD VDD VDD sky130_fd_pr__pfet_01v8 L=0.6 W=1.5 nf=1 ad='int((nf+1)/2) * W/nf * 0.29' as='int((nf+2)/2) * W/nf * 0.29'
+ pd='2*int((nf+1)/2) * (W/nf + 0.29)' ps='2*int((nf+2)/2) * (W/nf + 0.29)' nrd='0.29 / W' nrs='0.29 / W'
+ sa=0 sb=0 sd=0 mult=1 m=1
XMdummy11 GND GND GND GND sky130_fd_pr__nfet_01v8 L=0.6 W=1.5 nf=1 ad='int((nf+1)/2) * W/nf * 0.29' as='int((nf+2)/2) * W/nf * 0.29'
+ pd='2*int((nf+1)/2) * (W/nf + 0.29)' ps='2*int((nf+2)/2) * (W/nf + 0.29)' nrd='0.29 / W' nrs='0.29 / W'
+ sa=0 sb=0 sd=0 mult=1 m=1
XMdummy12 GND GND GND GND sky130_fd_pr__nfet_01v8 L=0.6 W=1.5 nf=1 ad='int((nf+1)/2) * W/nf * 0.29' as='int((nf+2)/2) * W/nf * 0.29'
+ pd='2*int((nf+1)/2) * (W/nf + 0.29)' ps='2*int((nf+2)/2) * (W/nf + 0.29)' nrd='0.29 / W' nrs='0.29 / W'
+ sa=0 sb=0 sd=0 mult=1 m=1
XMdummy21 GND GND GND GND sky130_fd_pr__nfet_01v8 L=0.6 W=1.5 nf=1 ad='int((nf+1)/2) * W/nf * 0.29' as='int((nf+2)/2) * W/nf * 0.29'
+ pd='2*int((nf+1)/2) * (W/nf + 0.29)' ps='2*int((nf+2)/2) * (W/nf + 0.29)' nrd='0.29 / W' nrs='0.29 / W'
+ sa=0 sb=0 sd=0 mult=1 m=1
XMdummy22 GND GND GND GND sky130_fd_pr__nfet_01v8 L=0.6 W=1.5 nf=1 ad='int((nf+1)/2) * W/nf * 0.29' as='int((nf+2)/2) * W/nf * 0.29'
+ pd='2*int((nf+1)/2) * (W/nf + 0.29)' ps='2*int((nf+2)/2) * (W/nf + 0.29)' nrd='0.29 / W' nrs='0.29 / W'
+ sa=0 sb=0 sd=0 mult=1 m=1
XM15 VDD GND GND GND sky130_fd_pr__nfet_01v8 L=0.6 W=1.5 nf=1 ad='int((nf+1)/2) * W/nf * 0.29' as='int((nf+2)/2) * W/nf * 0.29'
+ pd='2*int((nf+1)/2) * (W/nf + 0.29)' ps='2*int((nf+2)/2) * (W/nf + 0.29)' nrd='0.29 / W' nrs='0.29 / W'
+ sa=0 sb=0 sd=0 mult=1 m=1
XM16 GND GND VDD GND sky130_fd_pr__nfet_01v8 L=0.6 W=1.5 nf=1 ad='int((nf+1)/2) * W/nf * 0.29' as='int((nf+2)/2) * W/nf * 0.29'
+ pd='2*int((nf+1)/2) * (W/nf + 0.29)' ps='2*int((nf+2)/2) * (W/nf + 0.29)' nrd='0.29 / W' nrs='0.29 / W'
+ sa=0 sb=0 sd=0 mult=1 m=1
XM17 VDD VDD GND VDD sky130_fd_pr__pfet_01v8 L=0.6 W=1.5 nf=1 ad='int((nf+1)/2) * W/nf * 0.29' as='int((nf+2)/2) * W/nf * 0.29'
+ pd='2*int((nf+1)/2) * (W/nf + 0.29)' ps='2*int((nf+2)/2) * (W/nf + 0.29)' nrd='0.29 / W' nrs='0.29 / W'
+ sa=0 sb=0 sd=0 mult=1 m=1
XM18 GND VDD VDD VDD sky130_fd_pr__pfet_01v8 L=0.6 W=1.5 nf=1 ad='int((nf+1)/2) * W/nf * 0.29' as='int((nf+2)/2) * W/nf * 0.29'
+ pd='2*int((nf+1)/2) * (W/nf + 0.29)' ps='2*int((nf+2)/2) * (W/nf + 0.29)' nrd='0.29 / W' nrs='0.29 / W'
+ sa=0 sb=0 sd=0 mult=1 m=1
XMdummy23 GND GND GND GND sky130_fd_pr__nfet_01v8 L=0.6 W=1.5 nf=1 ad='int((nf+1)/2) * W/nf * 0.29' as='int((nf+2)/2) * W/nf * 0.29'
+ pd='2*int((nf+1)/2) * (W/nf + 0.29)' ps='2*int((nf+2)/2) * (W/nf + 0.29)' nrd='0.29 / W' nrs='0.29 / W'
+ sa=0 sb=0 sd=0 mult=1 m=1
XMdummy24 GND GND GND GND sky130_fd_pr__nfet_01v8 L=0.6 W=1.5 nf=1 ad='int((nf+1)/2) * W/nf * 0.29' as='int((nf+2)/2) * W/nf * 0.29'
+ pd='2*int((nf+1)/2) * (W/nf + 0.29)' ps='2*int((nf+2)/2) * (W/nf + 0.29)' nrd='0.29 / W' nrs='0.29 / W'
+ sa=0 sb=0 sd=0 mult=1 m=1
XM19 VDD VDD VDD VDD sky130_fd_pr__pfet_01v8 L=0.6 W=1.5 nf=1 ad='int((nf+1)/2) * W/nf * 0.29' as='int((nf+2)/2) * W/nf * 0.29'
+ pd='2*int((nf+1)/2) * (W/nf + 0.29)' ps='2*int((nf+2)/2) * (W/nf + 0.29)' nrd='0.29 / W' nrs='0.29 / W'
+ sa=0 sb=0 sd=0 mult=1 m=1
XMdummy25 GND GND GND GND sky130_fd_pr__nfet_01v8 L=0.6 W=1.5 nf=1 ad='int((nf+1)/2) * W/nf * 0.29' as='int((nf+2)/2) * W/nf * 0.29'
+ pd='2*int((nf+1)/2) * (W/nf + 0.29)' ps='2*int((nf+2)/2) * (W/nf + 0.29)' nrd='0.29 / W' nrs='0.29 / W'
+ sa=0 sb=0 sd=0 mult=1 m=1
XM20 VDD VDD VDD VDD sky130_fd_pr__pfet_01v8 L=0.6 W=1.5 nf=1 ad='int((nf+1)/2) * W/nf * 0.29' as='int((nf+2)/2) * W/nf * 0.29'
+ pd='2*int((nf+1)/2) * (W/nf + 0.29)' ps='2*int((nf+2)/2) * (W/nf + 0.29)' nrd='0.29 / W' nrs='0.29 / W'
+ sa=0 sb=0 sd=0 mult=1 m=1
XM21 VDD VDD VDD VDD sky130_fd_pr__pfet_01v8 L=0.6 W=1.5 nf=1 ad='int((nf+1)/2) * W/nf * 0.29' as='int((nf+2)/2) * W/nf * 0.29'
+ pd='2*int((nf+1)/2) * (W/nf + 0.29)' ps='2*int((nf+2)/2) * (W/nf + 0.29)' nrd='0.29 / W' nrs='0.29 / W'
+ sa=0 sb=0 sd=0 mult=1 m=1
XMdummy26 GND GND GND GND sky130_fd_pr__nfet_01v8 L=0.6 W=1.5 nf=1 ad='int((nf+1)/2) * W/nf * 0.29' as='int((nf+2)/2) * W/nf * 0.29'
+ pd='2*int((nf+1)/2) * (W/nf + 0.29)' ps='2*int((nf+2)/2) * (W/nf + 0.29)' nrd='0.29 / W' nrs='0.29 / W'
+ sa=0 sb=0 sd=0 mult=1 m=1
XM22 VDD VDD VDD VDD sky130_fd_pr__pfet_01v8 L=0.6 W=1.5 nf=1 ad='int((nf+1)/2) * W/nf * 0.29' as='int((nf+2)/2) * W/nf * 0.29'
+ pd='2*int((nf+1)/2) * (W/nf + 0.29)' ps='2*int((nf+2)/2) * (W/nf + 0.29)' nrd='0.29 / W' nrs='0.29 / W'
+ sa=0 sb=0 sd=0 mult=1 m=1
XM23 vout net10 VDD VDD sky130_fd_pr__pfet_01v8 L=0.15 W=12 nf=1 ad='int((nf+1)/2) * W/nf * 0.29' as='int((nf+2)/2) * W/nf * 0.29'
+ pd='2*int((nf+1)/2) * (W/nf + 0.29)' ps='2*int((nf+2)/2) * (W/nf + 0.29)' nrd='0.29 / W' nrs='0.29 / W'
+ sa=0 sb=0 sd=0 mult=1 m=1
XM24 vout net10 GND GND sky130_fd_pr__nfet_01v8 L=0.15 W=6 nf=1 ad='int((nf+1)/2) * W/nf * 0.29' as='int((nf+2)/2) * W/nf * 0.29'
+ pd='2*int((nf+1)/2) * (W/nf + 0.29)' ps='2*int((nf+2)/2) * (W/nf + 0.29)' nrd='0.29 / W' nrs='0.29 / W'
+ sa=0 sb=0 sd=0 mult=1 m=1
XC1 net10 vout sky130_fd_pr__cap_mim_m3_1 W=22 L=22 MF=1 m=1
**.ends
.GLOBAL VDD
.GLOBAL GND
.end
